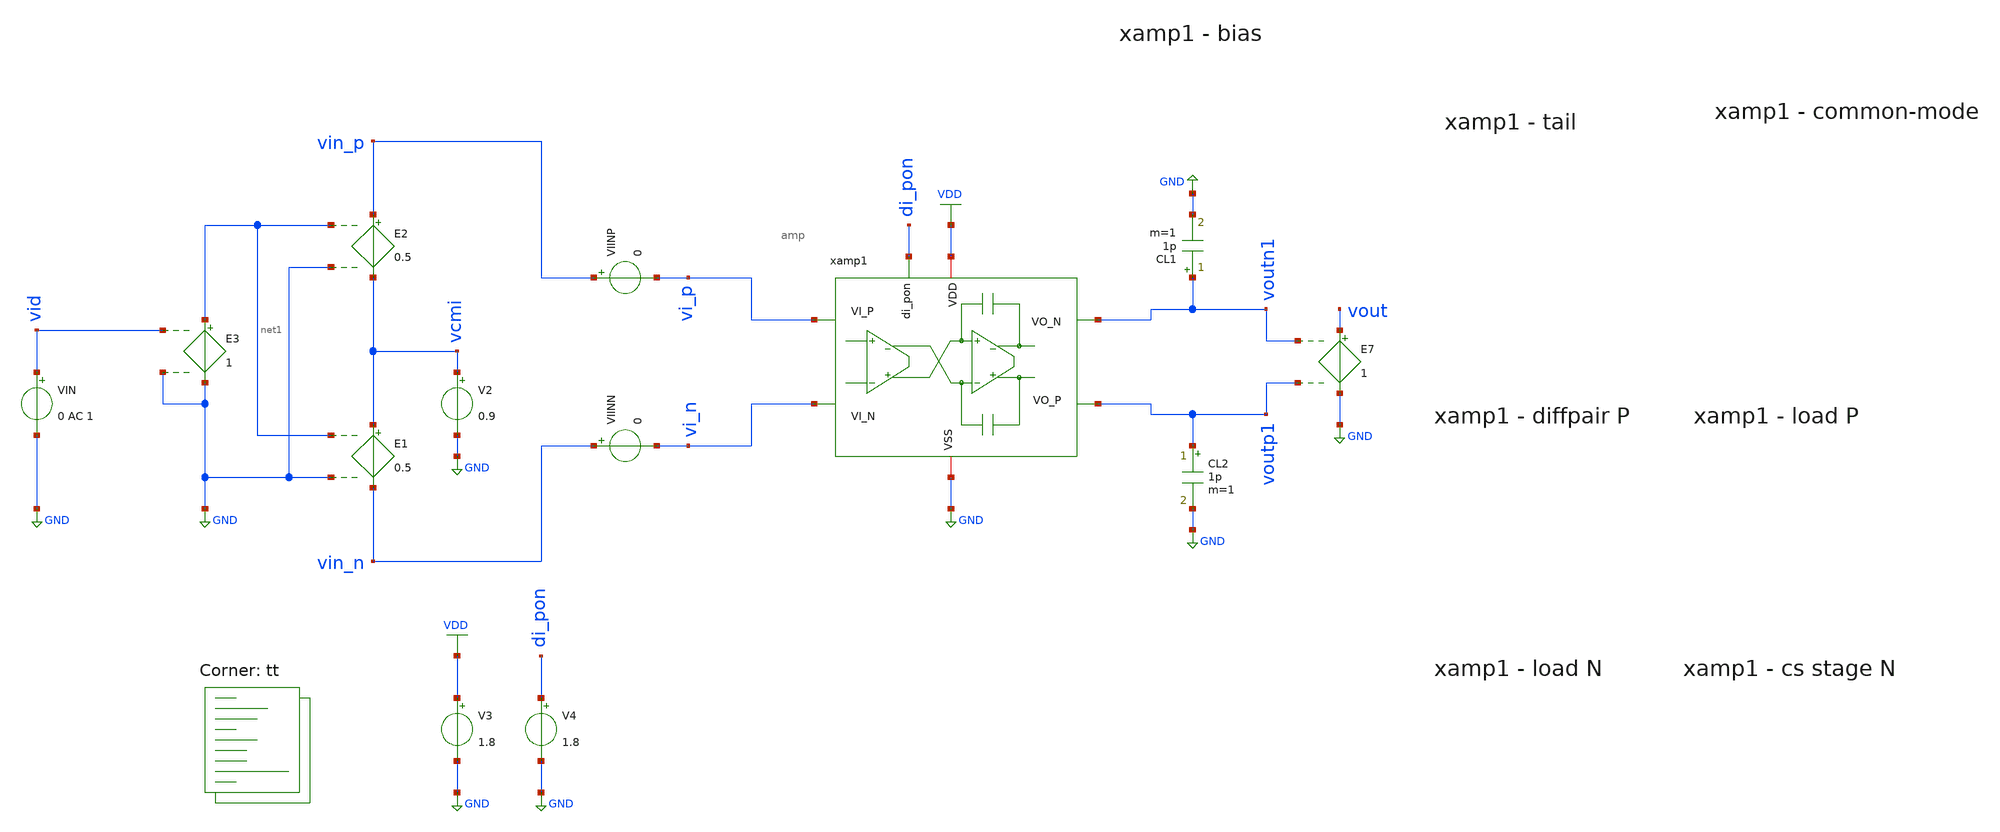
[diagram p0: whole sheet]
** sch_path: xschem/tb_amp_ol.sch
**.subckt tb_amp_ol
V3 VDD GND 1.8
V2 vcmi GND 0.9
E1 vcmi vin_n net1 GND 0.5
E2 vin_p vcmi net1 GND 0.5
VIN vid GND 0 AC 1
E3 net1 GND vid GND 1
VIINP vin_p vi_p 0
VIINN vin_n vi_n 0
V4 di_pon GND 1.8
E7 vout GND voutn1 voutp1 1
CL2 voutp1 GND 1p m=1
xamp1 VDD voutp1 di_pon vi_p vi_n voutn1 GND amp
CL1 voutn1 GND 1p m=1
**** begin user architecture code
.lib $::SKYWATER_MODELS/sky130.lib.spice tt


.include /foss/designs/amp_dev_sav.spice
.param CL=100f
.param CCM1=250f
.param CCM2=250f
.param VRREF=0.84
.param SCALE=5
.param IREF = {5u*SCALE}
.param RREF = {VRREF/IREF}
.param RCM = {100k}
.param WP = 5
.param WN = 3

.options savecurrents

.save all
.control
set doAmpSim = 0

if $doAmpSim eq 1
	setplot const
	let f_min = 10
	let f_max = 100Meg
	let f_stop = 500k

	let Adc = 2
	let v_step_o = 0.9
	let v_step_i = -v_step_o/Adc

	let t_rf = 0.01u
	let t_step = 50u
	let t_delay = 0
	let t_per = 2*t_step

	let tstep = 0.001*t_step
	let tstop = 2*t_per
	let tstart = t_delay

	alter @VIN[DC] = 0.0
	alter @VIN[PULSE] = [ 0 $&v_step_i $&t_delay $&t_rf $&t_rf $&t_step $&t_per 0 ]

	ac dec 100 $&const.f_min $&const.f_max

	noise v(vout) vin dec 100 $&const.f_min $&const.f_max

	tran $&tstep $&tstop $&tstart

	setplot ac1
	let Atot = v(vout)/v(vid)

	let Amag_ol_dB = vdb(Atot)
	let Aarg_ol = 180/PI*cphase(Atot)

	**let Amag_ol_dB_1 = vdb(A1)
	**let Aarg_ol_1 = 180/PI*cphase(A1)

	**let Amag_ol_dB_2 = vdb(A2)
	**let Aarg_ol_2 = 180/PI*cphase(A2)

	meas ac Amag_ol_dB max Amag_ol_dB
	let Amag_fc = Adc-3
	meas ac fc find frequency when Amag_ol_dB = Amag_fc
	meas ac fug_ol find frequency when Amag_ol_dB=0

	let Adc_ol_lin = 10^(Adc_ol/20)
	let err_gain = 1-Adc_ol_lin/(1+Adc_ol_lin)
	print err_gain*100

	plot Amag_ol_dB Aarg_ol ylabel 'Open Loop Magnitude, Phase'
	plot vdb(Acl) 180/PI*cphase(Acl)

	setplot noise1
	let acgain = onoise_spectrum/inoise_spectrum
	plot inoise_spectrum ylog xlog
	plot onoise_spectrum ylog xlog ylabel 'Output Noise'

	setplot noise2
	let p_noise_o = onoise_total^2
	let p_sig_o = v_step_o/sqrt(2)
	let snr = p_sig_o/p_noise_o
	let snr_dB = 10*log10(snr)

	setplot tran2
	let vcmo = (v(voutp1)+v(voutn1))/2
	plot v(vin_p) v(vin_n) v(voutp1) v(voutn1) vcmo
end

reset
op


*rm /foss/designs/filter/dc.txt
*show >> /foss/designs/filter/dc.txt
remzerovec
write tb_amp_ol.raw
.endc

**** end user architecture code
**.ends

* expanding   symbol:  /foss/designs/amp.sym # of pins=7
** sym_path: xschem/amp.sym
** sch_path: xschem/amp.sch
.subckt amp VDD VO_P di_pon VI_P VI_N VO_N VSS
*.iopin VSS
*.iopin VDD
*.ipin VI_P
*.ipin di_pon
*.ipin VI_N
*.opin VO_N
*.opin VO_P
XMP1 vbp vbp VDD VDD sky130_fd_pr__pfet_01v8 L=0.25 W='5 * 5 ' nf=5 ad='int((nf+1)/2) * W / nf * 0.29'
+ as='int((nf+2)/2) * W / nf * 0.29' pd='2*int((nf+1)/2) * (W / nf + 0.29)' ps='2*int((nf+2)/2) * (W / nf + 0.29)'
+ nrd='0.29 / W ' nrs='0.29 / W ' sa=0 sb=0 sd=0 mult=1 m=1
XMPSW3 vbp pon VDD VDD sky130_fd_pr__pfet_01v8 L=0.15 W='5 * 5 ' nf=5 ad='int((nf+1)/2) * W / nf * 0.29'
+ as='int((nf+2)/2) * W / nf * 0.29' pd='2*int((nf+1)/2) * (W / nf + 0.29)' ps='2*int((nf+2)/2) * (W / nf + 0.29)'
+ nrd='0.29 / W ' nrs='0.29 / W ' sa=0 sb=0 sd=0 mult=1 m=1
XMNSW1 pon_b di_pon VSS VSS sky130_fd_pr__nfet_01v8 L=0.15 W='3 * 1 ' nf=1 ad='int((nf+1)/2) * W / nf * 0.29'
+ as='int((nf+2)/2) * W / nf * 0.29' pd='2*int((nf+1)/2) * (W / nf + 0.29)' ps='2*int((nf+2)/2) * (W / nf + 0.29)'
+ nrd='0.29 / W ' nrs='0.29 / W ' sa=0 sb=0 sd=0 mult=1 m=1
XMPSW1 pon_b di_pon VDD VDD sky130_fd_pr__pfet_01v8 L=0.15 W='5 * 1 ' nf=1 ad='int((nf+1)/2) * W / nf * 0.29'
+ as='int((nf+2)/2) * W / nf * 0.29' pd='2*int((nf+1)/2) * (W / nf + 0.29)' ps='2*int((nf+2)/2) * (W / nf + 0.29)'
+ nrd='0.29 / W ' nrs='0.29 / W ' sa=0 sb=0 sd=0 mult=1 m=1
XMNSW2 pon pon_b VSS VSS sky130_fd_pr__nfet_01v8 L=0.15 W='3 * 3 ' nf=3 ad='int((nf+1)/2) * W / nf * 0.29'
+ as='int((nf+2)/2) * W / nf * 0.29' pd='2*int((nf+1)/2) * (W / nf + 0.29)' ps='2*int((nf+2)/2) * (W / nf + 0.29)'
+ nrd='0.29 / W ' nrs='0.29 / W ' sa=0 sb=0 sd=0 mult=1 m=1
XMPSW2 pon pon_b VDD VDD sky130_fd_pr__pfet_01v8 L=0.15 W='5 * 3 ' nf=3 ad='int((nf+1)/2) * W / nf * 0.29'
+ as='int((nf+2)/2) * W / nf * 0.29' pd='2*int((nf+1)/2) * (W / nf + 0.29)' ps='2*int((nf+2)/2) * (W / nf + 0.29)'
+ nrd='0.29 / W ' nrs='0.29 / W ' sa=0 sb=0 sd=0 mult=1 m=1
XMP2 viref1 vbp VDD VDD sky130_fd_pr__pfet_01v8 L=0.25 W='5 * 50 ' nf=50 ad='int((nf+1)/2) * W / nf * 0.29'
+ as='int((nf+2)/2) * W / nf * 0.29' pd='2*int((nf+1)/2) * (W / nf + 0.29)' ps='2*int((nf+2)/2) * (W / nf + 0.29)'
+ nrd='0.29 / W ' nrs='0.29 / W ' sa=0 sb=0 sd=0 mult=1 m=1
XMP3 vfb2 vbp VDD VDD sky130_fd_pr__pfet_01v8 L=0.25 W='5 * 5 ' nf=5 ad='int((nf+1)/2) * W / nf * 0.29'
+ as='int((nf+2)/2) * W / nf * 0.29' pd='2*int((nf+1)/2) * (W / nf + 0.29)' ps='2*int((nf+2)/2) * (W / nf + 0.29)'
+ nrd='0.29 / W ' nrs='0.29 / W ' sa=0 sb=0 sd=0 mult=1 m=1
XC6 VDD vbp sky130_fd_pr__cap_mim_m3_1 W=5 L=5 MF=5 m=5
XMP4 voutn1 VI_P viref1 viref1 sky130_fd_pr__pfet_01v8 L=0.15 W='5 * 20 ' nf=20 ad='int((nf+1)/2) * W / nf * 0.29'
+ as='int((nf+2)/2) * W / nf * 0.29' pd='2*int((nf+1)/2) * (W / nf + 0.29)' ps='2*int((nf+2)/2) * (W / nf + 0.29)'
+ nrd='0.29 / W ' nrs='0.29 / W ' sa=0 sb=0 sd=0 mult=1 m=1
XMP5 voutp1 VI_N viref1 viref1 sky130_fd_pr__pfet_01v8 L=0.15 W='5 * 20 ' nf=20 ad='int((nf+1)/2) * W / nf * 0.29'
+ as='int((nf+2)/2) * W / nf * 0.29' pd='2*int((nf+1)/2) * (W / nf + 0.29)' ps='2*int((nf+2)/2) * (W / nf + 0.29)'
+ nrd='0.29 / W ' nrs='0.29 / W ' sa=0 sb=0 sd=0 mult=1 m=1
XMN1 voutn1 vfb1 VSS VSS sky130_fd_pr__nfet_01v8 L=0.5 W='3 * 1 ' nf=1 ad='int((nf+1)/2) * W / nf * 0.29'
+ as='int((nf+2)/2) * W / nf * 0.29' pd='2*int((nf+1)/2) * (W / nf + 0.29)' ps='2*int((nf+2)/2) * (W / nf + 0.29)'
+ nrd='0.29 / W ' nrs='0.29 / W ' sa=0 sb=0 sd=0 mult=1 m=1
XMN2 voutp1 vfb1 VSS VSS sky130_fd_pr__nfet_01v8 L=0.5 W='3 * 1 ' nf=1 ad='int((nf+1)/2) * W / nf * 0.29'
+ as='int((nf+2)/2) * W / nf * 0.29' pd='2*int((nf+1)/2) * (W / nf + 0.29)' ps='2*int((nf+2)/2) * (W / nf + 0.29)'
+ nrd='0.29 / W ' nrs='0.29 / W ' sa=0 sb=0 sd=0 mult=1 m=1
R1 voutn1 vfb1 40k m=1
R3 vfb1 voutp1 40k m=1
XMN3 VO_P voutn1 net1 VSS sky130_fd_pr__nfet_01v8 L=0.5 W='3 * 1 ' nf=1 ad='int((nf+1)/2) * W / nf * 0.29'
+ as='int((nf+2)/2) * W / nf * 0.29' pd='2*int((nf+1)/2) * (W / nf + 0.29)' ps='2*int((nf+2)/2) * (W / nf + 0.29)'
+ nrd='0.29 / W ' nrs='0.29 / W ' sa=0 sb=0 sd=0 mult=1 m=1
XMN4 VO_N voutp1 VSS VSS sky130_fd_pr__nfet_01v8 L=0.5 W='3 * 1 ' nf=1 ad='int((nf+1)/2) * W / nf * 0.29'
+ as='int((nf+2)/2) * W / nf * 0.29' pd='2*int((nf+1)/2) * (W / nf + 0.29)' ps='2*int((nf+2)/2) * (W / nf + 0.29)'
+ nrd='0.29 / W ' nrs='0.29 / W ' sa=0 sb=0 sd=0 mult=1 m=1
XMP6 VO_P vfb2 VDD VDD sky130_fd_pr__pfet_01v8 L=0.25 W='5 * 10 ' nf=10 ad='int((nf+1)/2) * W / nf * 0.29'
+ as='int((nf+2)/2) * W / nf * 0.29' pd='2*int((nf+1)/2) * (W / nf + 0.29)' ps='2*int((nf+2)/2) * (W / nf + 0.29)'
+ nrd='0.29 / W ' nrs='0.29 / W ' sa=0 sb=0 sd=0 mult=1 m=1
XMP7 VO_N vfb2 VDD VDD sky130_fd_pr__pfet_01v8 L=0.25 W='5 * 10 ' nf=10 ad='int((nf+1)/2) * W / nf * 0.29'
+ as='int((nf+2)/2) * W / nf * 0.29' pd='2*int((nf+1)/2) * (W / nf + 0.29)' ps='2*int((nf+2)/2) * (W / nf + 0.29)'
+ nrd='0.29 / W ' nrs='0.29 / W ' sa=0 sb=0 sd=0 mult=1 m=1
XC1 voutn1 vfb1 sky130_fd_pr__cap_mim_m3_1 W=5 L=5 MF=5 m=5
XC2 vfb1 voutp1 sky130_fd_pr__cap_mim_m3_1 W=5 L=5 MF=5 m=5
I0 vbp VSS 10u
R2 VO_P vfb2 40k m=1
R4 vfb2 VO_N 40k m=1
XC3 VO_P vfb2 sky130_fd_pr__cap_mim_m3_1 W=5 L=5 MF=5 m=5
XC4 vfb2 VO_N sky130_fd_pr__cap_mim_m3_1 W=5 L=5 MF=5 m=5
.ends

.GLOBAL GND
.GLOBAL VDD
.end
